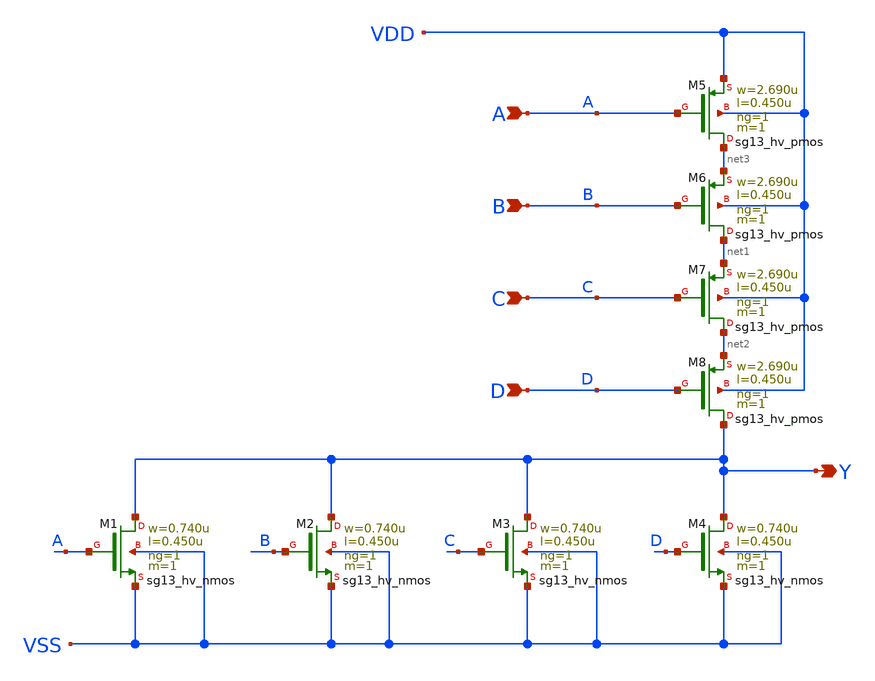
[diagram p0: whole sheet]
** sch_path: ihp-sg13g2/libs.ref/sg13g2_stdcell_hv/sch/xschem/sg13g2_hv_nor4_1.sch
* Copyright 2023 IHP PDK Authors
* Licensed under the Apache License, Version 2.0 (the "License");
* you may not use this file except in compliance with the License.
* You may obtain a copy of the License at
* https://www.apache.org/licenses/LICENSE-2.0
* Unless required by applicable law or agreed to in writing, software
* distributed under the License is distributed on an "AS IS" BASIS,
* WITHOUT WARRANTIES OR CONDITIONS OF ANY KIND, either express or implied.
* See the License for the specific language governing permissions and
* limitations under the License.
**.subckt sg13g2_hv_nor4_1 Y A B C D
*.opin Y
*.ipin A
*.ipin B
*.ipin C
*.ipin D
XM1 Y A VSS VSS sg13_hv_nmos w=0.740u l=0.450u ng=1 m=1 mm_ok=1
XM2 Y B VSS VSS sg13_hv_nmos w=0.740u l=0.450u ng=1 m=1 mm_ok=1
XM3 Y C VSS VSS sg13_hv_nmos w=0.740u l=0.450u ng=1 m=1 mm_ok=1
XM4 Y D VSS VSS sg13_hv_nmos w=0.740u l=0.450u ng=1 m=1 mm_ok=1
XM5 net3 A VDD VDD sg13_hv_pmos w=2.690u l=0.450u ng=1 m=1 mm_ok=1
XM6 net1 B net3 VDD sg13_hv_pmos w=2.690u l=0.450u ng=1 m=1 mm_ok=1
XM7 net2 C net1 VDD sg13_hv_pmos w=2.690u l=0.450u ng=1 m=1 mm_ok=1
XM8 Y D net2 VDD sg13_hv_pmos w=2.690u l=0.450u ng=1 m=1 mm_ok=1
**.ends
.end
